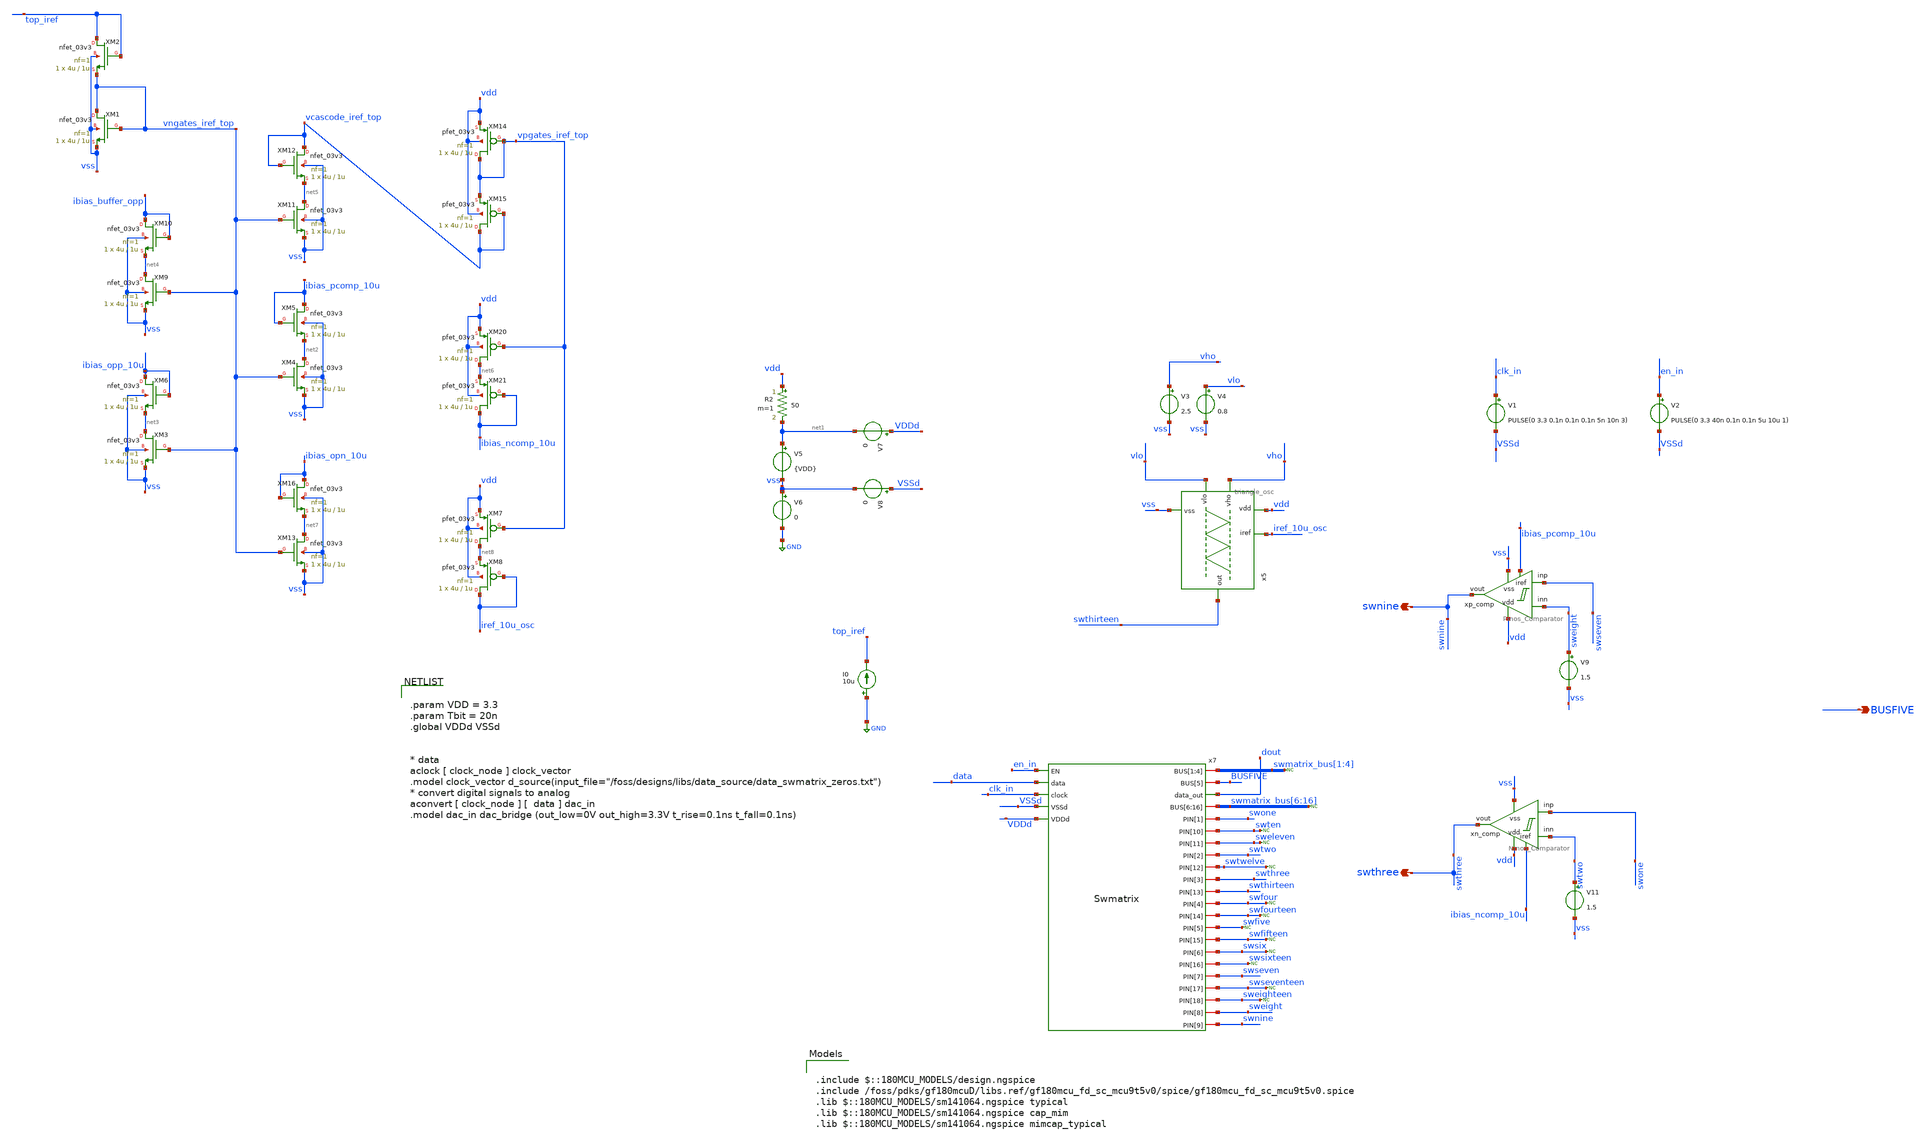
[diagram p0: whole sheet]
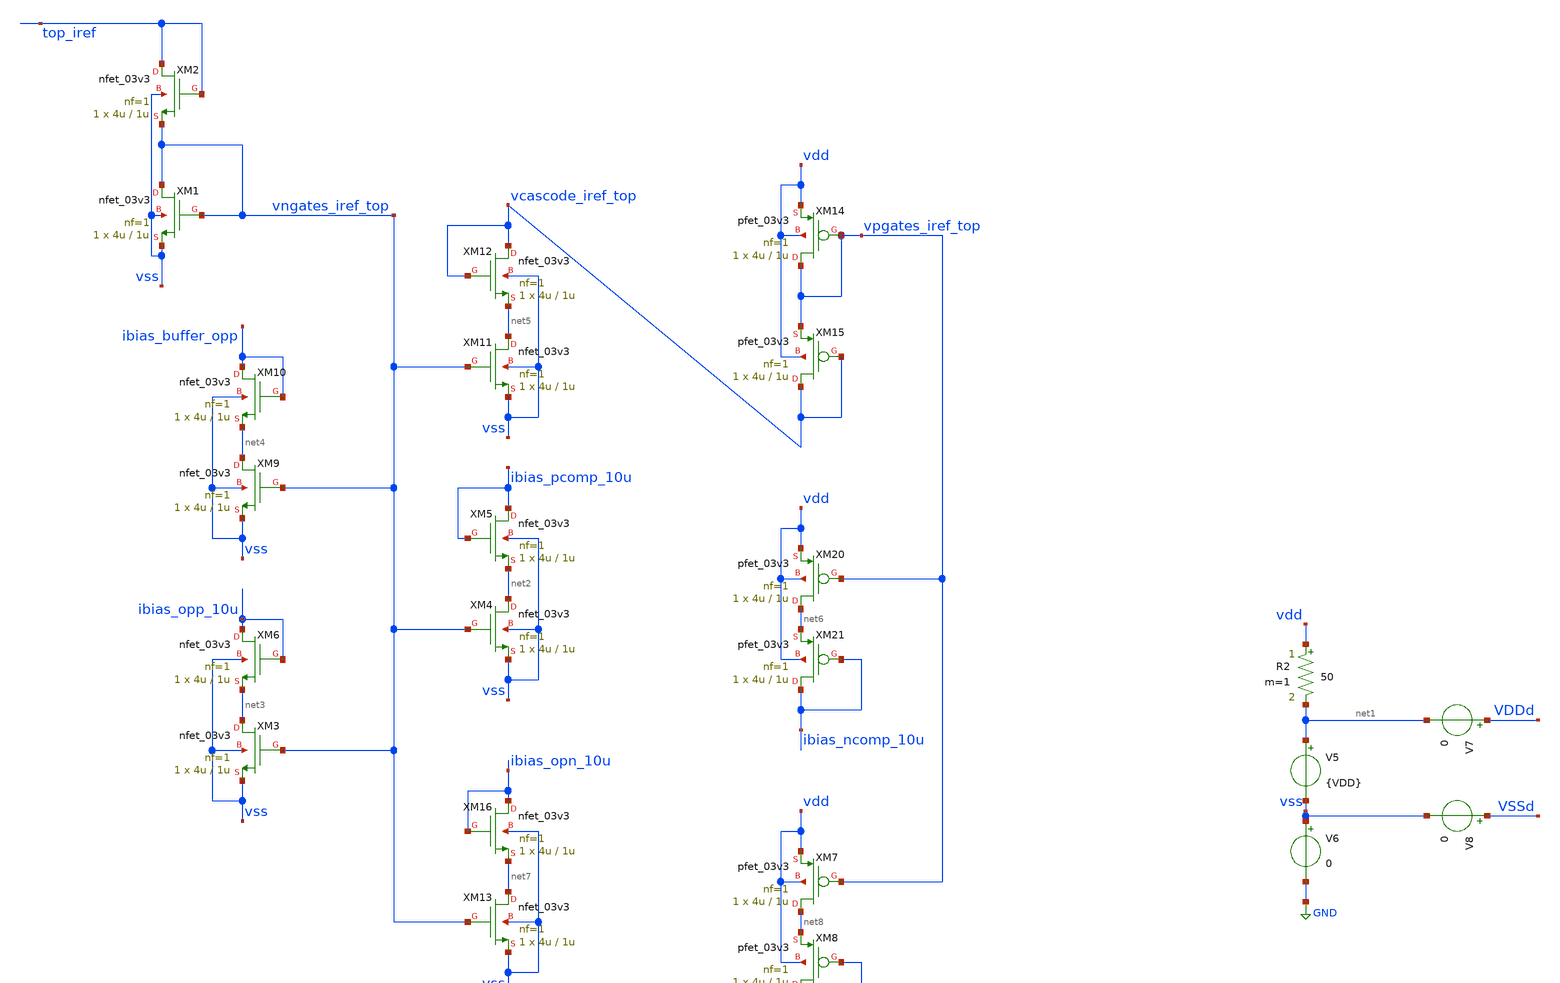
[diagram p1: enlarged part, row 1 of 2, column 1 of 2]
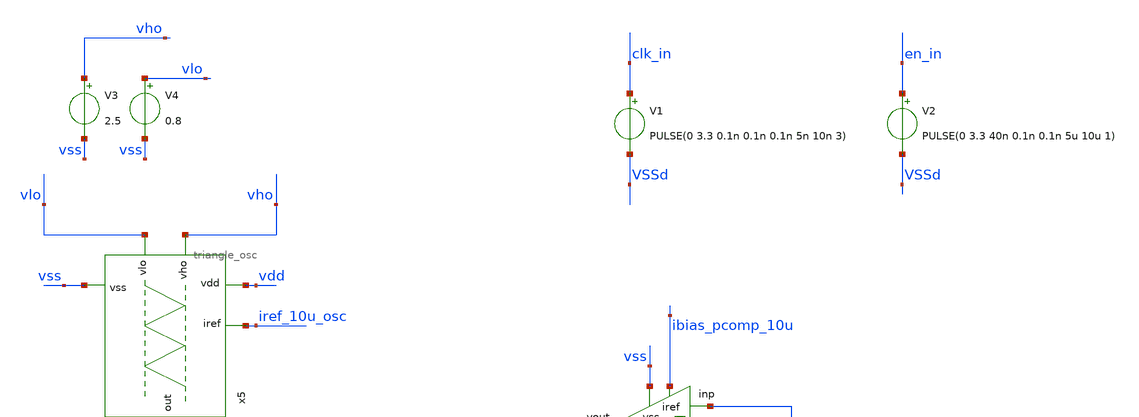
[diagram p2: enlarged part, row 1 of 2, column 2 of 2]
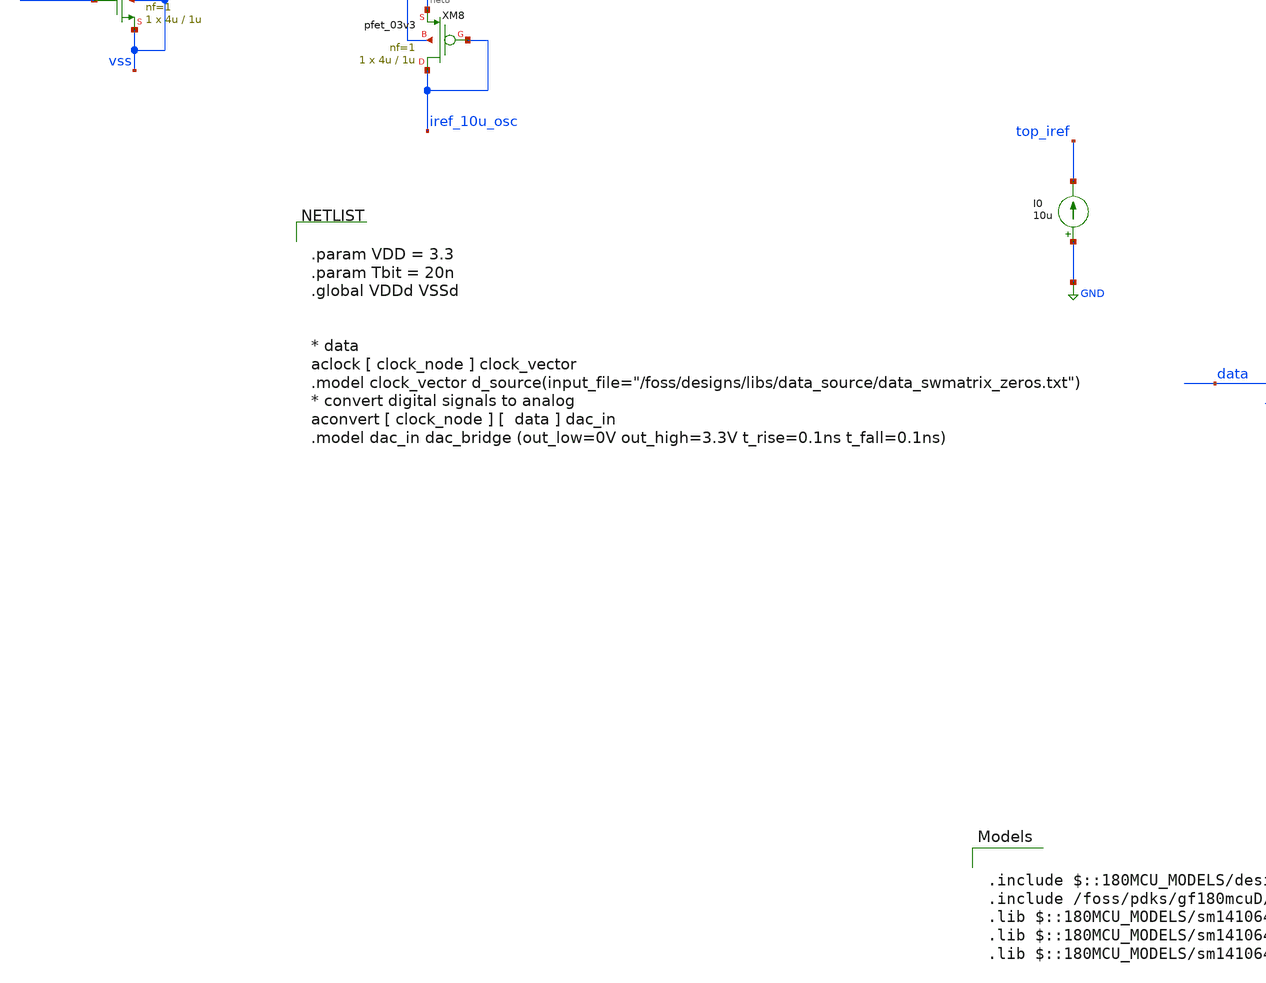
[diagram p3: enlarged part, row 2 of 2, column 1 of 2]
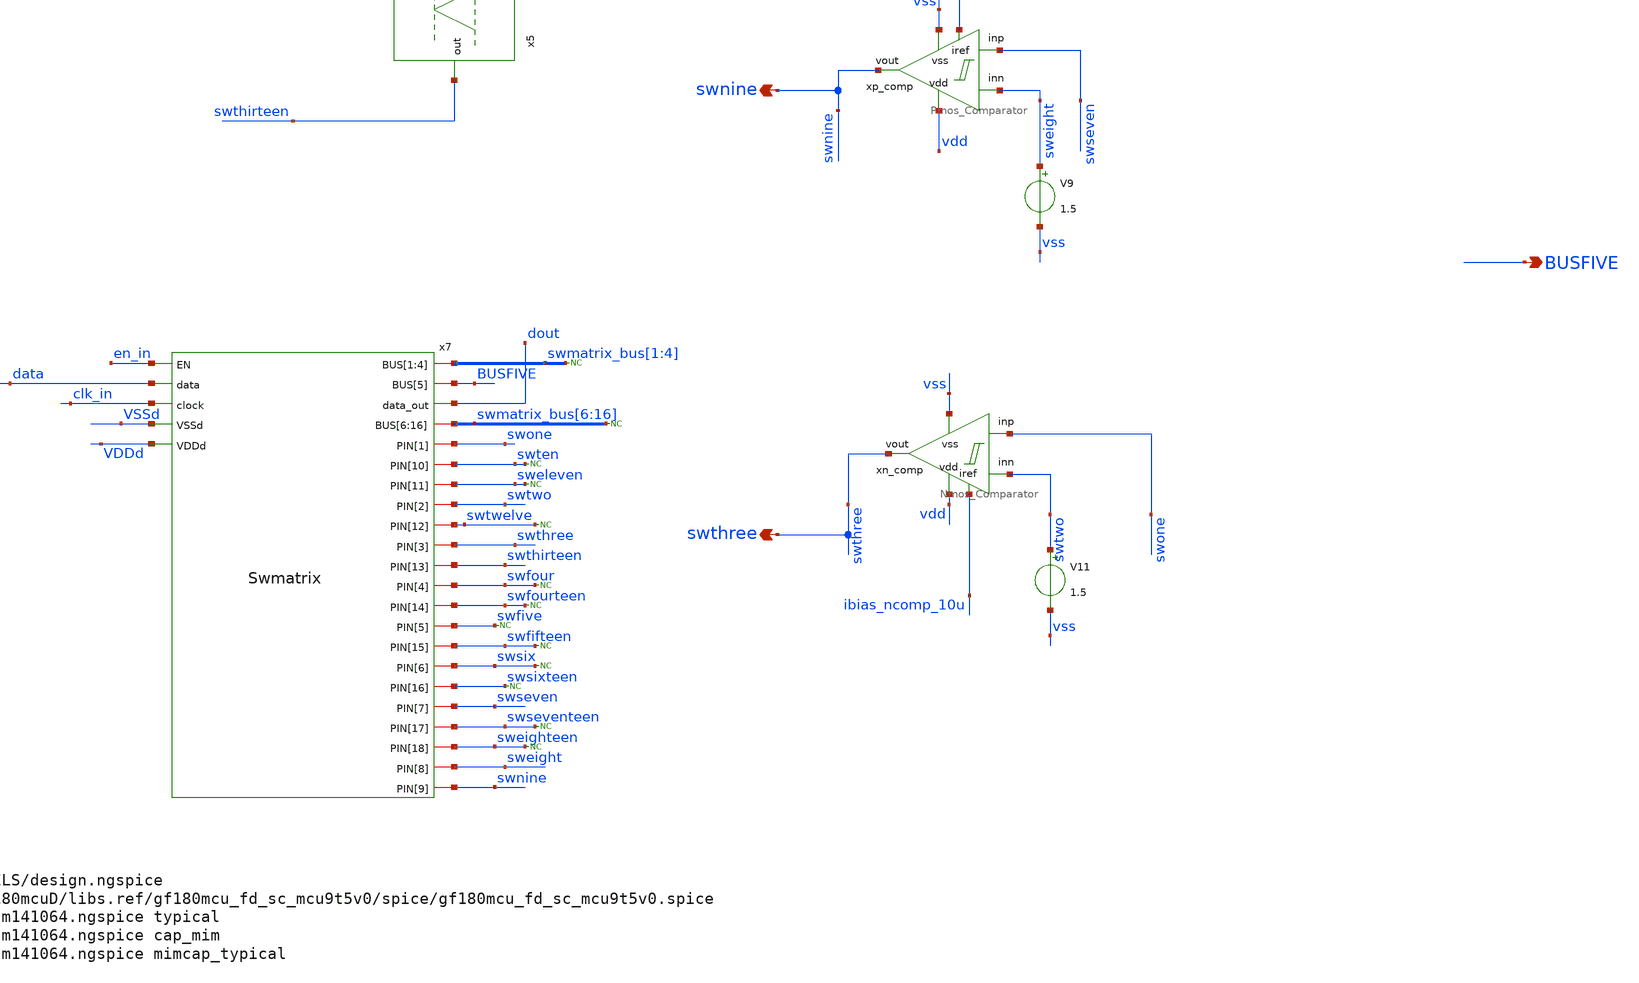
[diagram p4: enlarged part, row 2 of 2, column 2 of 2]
** sch_path: designs/libs/top_sim/deepstate.sch
**.subckt deepstate BUSFIVE swthree swnine
*.opin BUSFIVE
*.opin swthree
*.opin swnine
x7 en_in data swmatrix_bus[1] swmatrix_bus[2] swmatrix_bus[3] swmatrix_bus[4] BUSFIVE clk_in dout
+ swmatrix_bus[6] swmatrix_bus[7] swmatrix_bus[8] swmatrix_bus[9] swmatrix_bus[10] swmatrix_bus[11] swmatrix_bus[12]
+ swmatrix_bus[13] swmatrix_bus[14] swmatrix_bus[15] swmatrix_bus[16] swone swten sweleven swtwo swtwelve swthree
+ swthirteen swfour swfourteen swfive swfifteen swsix swsixteen swseven VSSd swseventeen sweighteen sweight VDDd
+ swnine Swmatrix
I0 GND top_iref 10u
V5 net1 vss {VDD}
V6 vss GND 0
V7 VDDd net1 0
V8 VSSd vss 0
R2 vdd net1 50 m=1
V9 sweight vss 1.5
xp_comp vdd swnine swseven vss sweight ibias_pcomp_10u Pmos_Comparator
xn_comp vdd swthree swone vss swtwo ibias_ncomp_10u Nmos_Comparator
V11 swtwo vss 1.5
x5 vdd vho swthirteen vlo iref_10u_osc vss triangle_osc
V3 vho vss 2.5
V4 vlo vss 0.8
* noconn swmatrix_bus[1:4]
* noconn swmatrix_bus[6:16]
* noconn swten
* noconn sweleven
* noconn swtwelve
* noconn swfour
* noconn swfourteen
* noconn swfive
* noconn swfifteen
* noconn swsix
* noconn swsixteen
* noconn swseventeen
* noconn sweighteen
V1 clk_in VSSd PULSE(0 3.3 0.1n 0.1n 0.1n 5n 10n 3)
V2 en_in VSSd PULSE(0 3.3 40n 0.1n 0.1n 5u 10u 1)
XM1 vngates_iref_top vngates_iref_top vss vss nfet_03v3 L=1u W=4u nf=1 ad='int((nf+1)/2) * W/nf * 0.18u'
+ as='int((nf+2)/2) * W/nf * 0.18u' pd='2*int((nf+1)/2) * (W/nf + 0.18u)' ps='2*int((nf+2)/2) * (W/nf + 0.18u)'
+ nrd='0.18u / W' nrs='0.18u / W' sa=0 sb=0 sd=0 m=1
XM2 top_iref top_iref vngates_iref_top vss nfet_03v3 L=1u W=4u nf=1 ad='int((nf+1)/2) * W/nf * 0.18u'
+ as='int((nf+2)/2) * W/nf * 0.18u' pd='2*int((nf+1)/2) * (W/nf + 0.18u)' ps='2*int((nf+2)/2) * (W/nf + 0.18u)'
+ nrd='0.18u / W' nrs='0.18u / W' sa=0 sb=0 sd=0 m=1
XM4 net2 vngates_iref_top vss vss nfet_03v3 L=1u W=4u nf=1 ad='int((nf+1)/2) * W/nf * 0.18u' as='int((nf+2)/2) * W/nf * 0.18u'
+ pd='2*int((nf+1)/2) * (W/nf + 0.18u)' ps='2*int((nf+2)/2) * (W/nf + 0.18u)' nrd='0.18u / W' nrs='0.18u / W'
+ sa=0 sb=0 sd=0 m=1
XM5 ibias_pcomp_10u ibias_pcomp_10u net2 vss nfet_03v3 L=1u W=4u nf=1 ad='int((nf+1)/2) * W/nf * 0.18u'
+ as='int((nf+2)/2) * W/nf * 0.18u' pd='2*int((nf+1)/2) * (W/nf + 0.18u)' ps='2*int((nf+2)/2) * (W/nf + 0.18u)'
+ nrd='0.18u / W' nrs='0.18u / W' sa=0 sb=0 sd=0 m=1
XM3 net3 vngates_iref_top vss vss nfet_03v3 L=1u W=4u nf=1 ad='int((nf+1)/2) * W/nf * 0.18u' as='int((nf+2)/2) * W/nf * 0.18u'
+ pd='2*int((nf+1)/2) * (W/nf + 0.18u)' ps='2*int((nf+2)/2) * (W/nf + 0.18u)' nrd='0.18u / W' nrs='0.18u / W'
+ sa=0 sb=0 sd=0 m=1
XM6 ibias_opp_10u ibias_opp_10u net3 vss nfet_03v3 L=1u W=4u nf=1 ad='int((nf+1)/2) * W/nf * 0.18u' as='int((nf+2)/2) * W/nf * 0.18u'
+ pd='2*int((nf+1)/2) * (W/nf + 0.18u)' ps='2*int((nf+2)/2) * (W/nf + 0.18u)' nrd='0.18u / W' nrs='0.18u / W'
+ sa=0 sb=0 sd=0 m=1
XM9 net4 vngates_iref_top vss vss nfet_03v3 L=1u W=4u nf=1 ad='int((nf+1)/2) * W/nf * 0.18u' as='int((nf+2)/2) * W/nf * 0.18u'
+ pd='2*int((nf+1)/2) * (W/nf + 0.18u)' ps='2*int((nf+2)/2) * (W/nf + 0.18u)' nrd='0.18u / W' nrs='0.18u / W'
+ sa=0 sb=0 sd=0 m=1
XM10 ibias_buffer_opp ibias_buffer_opp net4 vss nfet_03v3 L=1u W=4u nf=1 ad='int((nf+1)/2) * W/nf * 0.18u'
+ as='int((nf+2)/2) * W/nf * 0.18u' pd='2*int((nf+1)/2) * (W/nf + 0.18u)' ps='2*int((nf+2)/2) * (W/nf + 0.18u)'
+ nrd='0.18u / W' nrs='0.18u / W' sa=0 sb=0 sd=0 m=1
XM11 net5 vngates_iref_top vss vss nfet_03v3 L=1u W=4u nf=1 ad='int((nf+1)/2) * W/nf * 0.18u' as='int((nf+2)/2) * W/nf * 0.18u'
+ pd='2*int((nf+1)/2) * (W/nf + 0.18u)' ps='2*int((nf+2)/2) * (W/nf + 0.18u)' nrd='0.18u / W' nrs='0.18u / W'
+ sa=0 sb=0 sd=0 m=1
XM12 vcascode_iref_top vcascode_iref_top net5 vss nfet_03v3 L=1u W=4u nf=1 ad='int((nf+1)/2) * W/nf * 0.18u'
+ as='int((nf+2)/2) * W/nf * 0.18u' pd='2*int((nf+1)/2) * (W/nf + 0.18u)' ps='2*int((nf+2)/2) * (W/nf + 0.18u)'
+ nrd='0.18u / W' nrs='0.18u / W' sa=0 sb=0 sd=0 m=1
XM14 vpgates_iref_top vpgates_iref_top vdd vdd pfet_03v3 L=1u W=4u nf=1 ad='int((nf+1)/2) * W/nf * 0.18u'
+ as='int((nf+2)/2) * W/nf * 0.18u' pd='2*int((nf+1)/2) * (W/nf + 0.18u)' ps='2*int((nf+2)/2) * (W/nf + 0.18u)'
+ nrd='0.18u / W' nrs='0.18u / W' sa=0 sb=0 sd=0 m=1
XM15 vcascode_iref_top vcascode_iref_top vpgates_iref_top vdd pfet_03v3 L=1u W=4u nf=1 ad='int((nf+1)/2) * W/nf * 0.18u'
+ as='int((nf+2)/2) * W/nf * 0.18u' pd='2*int((nf+1)/2) * (W/nf + 0.18u)' ps='2*int((nf+2)/2) * (W/nf + 0.18u)'
+ nrd='0.18u / W' nrs='0.18u / W' sa=0 sb=0 sd=0 m=1
XM20 net6 vpgates_iref_top vdd vdd pfet_03v3 L=1u W=4u nf=1 ad='int((nf+1)/2) * W/nf * 0.18u' as='int((nf+2)/2) * W/nf * 0.18u'
+ pd='2*int((nf+1)/2) * (W/nf + 0.18u)' ps='2*int((nf+2)/2) * (W/nf + 0.18u)' nrd='0.18u / W' nrs='0.18u / W'
+ sa=0 sb=0 sd=0 m=1
XM21 ibias_ncomp_10u ibias_ncomp_10u net6 vdd pfet_03v3 L=1u W=4u nf=1 ad='int((nf+1)/2) * W/nf * 0.18u'
+ as='int((nf+2)/2) * W/nf * 0.18u' pd='2*int((nf+1)/2) * (W/nf + 0.18u)' ps='2*int((nf+2)/2) * (W/nf + 0.18u)'
+ nrd='0.18u / W' nrs='0.18u / W' sa=0 sb=0 sd=0 m=1
XM13 net7 vngates_iref_top vss vss nfet_03v3 L=1u W=4u nf=1 ad='int((nf+1)/2) * W/nf * 0.18u' as='int((nf+2)/2) * W/nf * 0.18u'
+ pd='2*int((nf+1)/2) * (W/nf + 0.18u)' ps='2*int((nf+2)/2) * (W/nf + 0.18u)' nrd='0.18u / W' nrs='0.18u / W'
+ sa=0 sb=0 sd=0 m=1
XM16 ibias_opn_10u ibias_opn_10u net7 vss nfet_03v3 L=1u W=4u nf=1 ad='int((nf+1)/2) * W/nf * 0.18u'
+ as='int((nf+2)/2) * W/nf * 0.18u' pd='2*int((nf+1)/2) * (W/nf + 0.18u)' ps='2*int((nf+2)/2) * (W/nf + 0.18u)'
+ nrd='0.18u / W' nrs='0.18u / W' sa=0 sb=0 sd=0 m=1
XM7 net8 vpgates_iref_top vdd vdd pfet_03v3 L=1u W=4u nf=1 ad='int((nf+1)/2) * W/nf * 0.18u' as='int((nf+2)/2) * W/nf * 0.18u'
+ pd='2*int((nf+1)/2) * (W/nf + 0.18u)' ps='2*int((nf+2)/2) * (W/nf + 0.18u)' nrd='0.18u / W' nrs='0.18u / W'
+ sa=0 sb=0 sd=0 m=1
XM8 iref_10u_osc iref_10u_osc net8 vdd pfet_03v3 L=1u W=4u nf=1 ad='int((nf+1)/2) * W/nf * 0.18u' as='int((nf+2)/2) * W/nf * 0.18u'
+ pd='2*int((nf+1)/2) * (W/nf + 0.18u)' ps='2*int((nf+2)/2) * (W/nf + 0.18u)' nrd='0.18u / W' nrs='0.18u / W'
+ sa=0 sb=0 sd=0 m=1
**** begin user architecture code

.include $::180MCU_MODELS/design.ngspice
.include /foss/pdks/gf180mcuD/libs.ref/gf180mcu_fd_sc_mcu9t5v0/spice/gf180mcu_fd_sc_mcu9t5v0.spice
.lib $::180MCU_MODELS/sm141064.ngspice typical
.lib $::180MCU_MODELS/sm141064.ngspice cap_mim
.lib $::180MCU_MODELS/sm141064.ngspice mimcap_typical




.control
    save clk_in
    save data
    save en_in
    save v(x7.x2.xangel_row_block[1].xSR.xFF[1].out_m)
    save v(x7.x2.xangel_row_block[1].xSR.xFF[1].s)
    save v(x7.x2.xangel_row_block[1].xSR.xFF[2].out_m)
    save v(x7.x2.xangel_row_block[1].xSR.xFF[2].s)
    save v(x7.x2.xangel_row_block[1].xSR.xFF[3].out_m)
    save v(x7.x2.xangel_row_block[1].xSR.xFF[3].s)
    save v(x7.x2.xangel_row_block[1].xSR.xFF[4].out_m)
    save v(x7.x2.xangel_row_block[1].xSR.xFF[4].s)
    save v(x7.x2.xangel_row_block[1].xSR.xFF[5].out_m)
    save v(x7.x2.xangel_row_block[1].xSR.xFF[5].s)
    save v(x7.x2.xangel_row_block[1].xSR.xFF[6].out_m)
    save v(x7.x2.xangel_row_block[1].xSR.xFF[6].s)

    save v(x7.x2.xangel_row_block[7].xSR.xFF[1].out_m)
    save v(x7.x2.xangel_row_block[7].xSR.xFF[1].s)
    save v(x7.x2.xangel_row_block[7].xSR.xFF[2].out_m)
    save v(x7.x2.xangel_row_block[7].xSR.xFF[2].s)
    save v(x7.x2.xangel_row_block[13].xSR.xFF[1].out_m)
    save v(x7.x2.xangel_row_block[13].xSR.xFF[1].s)
    save v(x7.x2.xangel_row_block[13].xSR.xFF[2].out_m)
    save v(x7.x2.xangel_row_block[13].xSR.xFF[2].s)
    save v(x7.x2.xangel_row_block[13].xSR.xFF[4].out_m)
    save v(x7.x2.xangel_row_block[13].xSR.xFF[4].s)
    save v(x7.x2.xangel_row_block[13].xSR.xFF[5].out_m)
    save v(x7.x2.xangel_row_block[13].xSR.xFF[5].s)
    save swone swtwo swthree swseven swnine swthirteen BUSFIVE
    TRAN 2n 120n
    write deepstate.raw

.endc




.param VDD = 3.3
.param Tbit = 20n
.global VDDd VSSd


* data
aclock [ clock_node ] clock_vector
.model clock_vector d_source(input_file="/foss/designs/libs/data_source/data_swmatrix_zeros.txt")
* convert digital signals to analog
aconvert [ clock_node ] [  data ] dac_in
.model dac_in dac_bridge (out_low=0V out_high=3.3V t_rise=0.1ns t_fall=0.1ns)


**** end user architecture code
**.ends
.GLOBAL GND
.end
